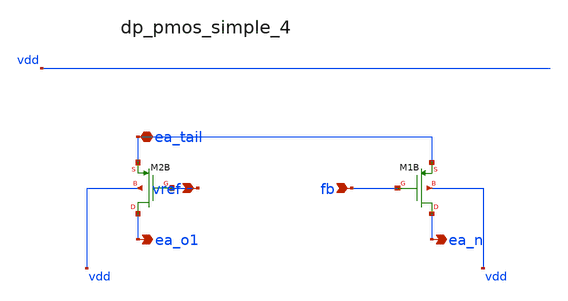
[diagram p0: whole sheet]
** sch_path: analog-db/raw/ldo_010_capless_lowiq/hier/blocks/dp_pmos_simple_4.sch
**.subckt dp_pmos_simple_4 vref fb ea_tail ea_o1 ea_n
*.ipin vref
*.ipin fb
*.iopin ea_tail
*.opin ea_o1
*.opin ea_n
XM1B ea_n fb ea_tail vdd sg13_lv_pmos w={x_dut_xm1_w/2} l=x_dut_xm1_l ng=1 m=1
XM2B ea_o1 vref ea_tail vdd sg13_lv_pmos w={x_dut_xm1_w/2} l=x_dut_xm1_l ng=1 m=1
**.ends
.end
